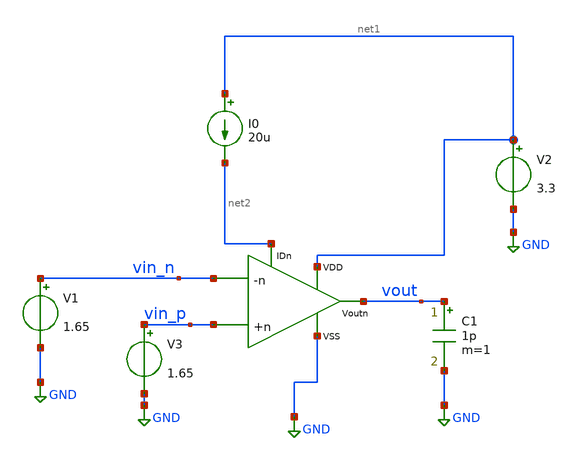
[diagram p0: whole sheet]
** sch_path: xschem/ota_miller/prueba_lazo_abierto_ota_n.sch
**.subckt prueba_lazo_abierto_ota_n
V1 vin_n GND 1.65
V2 net1 GND 3.3
C1 vout GND 1p m=1
V3 vin_p GND 1.65
I0 net1 net2 20u
x1 net1 vout net2 vin_n vin_p GND ota_n_in
**** begin user architecture code


.control
save all
* Coloracion de graficas
set color0=white
set color1=black
set color2=blue
set color3=red
set xbrushwidth=2

* 1. Senoidales en contrafase alrededor de 1.65V (amplitud 50uV para no saturar)
alter @v1[sin] [ 1.65 50u 1k 0 0 180 ]
alter @v3[sin] [ 1.65 50u 1k 0 0 0 ]

* 2. Simular 5 ms con paso de 1 us (5 ciclos de 1 kHz)
tran 1u 5m

* 3. Calcular diferencia de entrada y sus valores pico a pico
let vdiff = v(vin_p) - v(vin_n)
let vdiff_max = vecmax(vdiff)
let vdiff_min = vecmin(vdiff)
let vdiff_pp = vdiff_max - vdiff_min

* 4. Medir pico a pico, valor promedio DC y offset respecto a 1.65V (en 3 ciclos: 2ms a 5ms)
meas tran vout_pp pp v(vout) from=2m to=5m
meas tran vout_dc avg v(vout) from=2m to=5m

let Av0 = vout_pp / vdiff_pp
let Av0_dB = 20 * log10(Av0)
let offset_out = vout_dc - 1.65
let offset_in = offset_out / Av0

echo ========================================
print vdiff_pp
print vout_pp
print Av0
print Av0_dB
print vout_dc
print offset_out
print offset_in
echo ========================================

* 5. Graficas por separado: salida y senal diferencial
plot v(vout) title 'Salida OTA (Lazo Abierto)' xlabel 'Tiempo (s)' ylabel 'Voltaje (V)'
plot vdiff title 'Senal Diferencial de Entrada (V+ - V-)' xlabel 'Tiempo (s)' ylabel 'Voltaje (V)'
.endc




.include /home/ringosinye/eda/pdks/gf180mcuD/libs.tech/ngspice/design.ngspice
.lib /home/ringosinye/eda/pdks/gf180mcuD/libs.tech/ngspice/sm141064.ngspice typical
.param sw_stat_mismatch = 0


**** end user architecture code
**.ends

* expanding   symbol:  ota_n_in.sym # of pins=6
** sym_path: xschem/ota_miller/ota_n_in.sym
** sch_path: xschem/ota_miller/ota_n_in.sch
.subckt ota_n_in VDD Voutn IDn -n +n VSS
*.opin Voutn
*.ipin VSS
*.ipin VDD
*.ipin +n
*.ipin -n
*.ipin IDn
XM1 net2 +n net1 GND nfet_03v3 L=1u W=4.1u nf=1 ad='int((nf+1)/2) * W/nf * 0.18u' as='int((nf+2)/2) * W/nf * 0.18u'
+ pd='2*int((nf+1)/2) * (W/nf + 0.18u)' ps='2*int((nf+2)/2) * (W/nf + 0.18u)' nrd='0.18u / W' nrs='0.18u / W'
+ sa=0 sb=0 sd=0 m=1 par=1
XM2 Voutn -n net1 GND nfet_03v3 L=1u W=4.1u nf=1 ad='int((nf+1)/2) * W/nf * 0.18u' as='int((nf+2)/2) * W/nf * 0.18u'
+ pd='2*int((nf+1)/2) * (W/nf + 0.18u)' ps='2*int((nf+2)/2) * (W/nf + 0.18u)' nrd='0.18u / W' nrs='0.18u / W'
+ sa=0 sb=0 sd=0 m=1 par=1
XM3 net2 net2 VDD VDD pfet_03v3 L=1u W=10u nf=1 ad='int((nf+1)/2) * W/nf * 0.18u' as='int((nf+2)/2) * W/nf * 0.18u'
+ pd='2*int((nf+1)/2) * (W/nf + 0.18u)' ps='2*int((nf+2)/2) * (W/nf + 0.18u)' nrd='0.18u / W' nrs='0.18u / W'
+ sa=0 sb=0 sd=0 m=1 par=1
XM4 Voutn net2 VDD VDD pfet_03v3 L=1u W=10u nf=1 ad='int((nf+1)/2) * W/nf * 0.18u' as='int((nf+2)/2) * W/nf * 0.18u'
+ pd='2*int((nf+1)/2) * (W/nf + 0.18u)' ps='2*int((nf+2)/2) * (W/nf + 0.18u)' nrd='0.18u / W' nrs='0.18u / W'
+ sa=0 sb=0 sd=0 m=1 par=1
XM5 net1 IDn VSS GND nfet_03v3 L=1u W=5u nf=1 ad='int((nf+1)/2) * W/nf * 0.18u' as='int((nf+2)/2) * W/nf * 0.18u'
+ pd='2*int((nf+1)/2) * (W/nf + 0.18u)' ps='2*int((nf+2)/2) * (W/nf + 0.18u)' nrd='0.18u / W' nrs='0.18u / W'
+ sa=0 sb=0 sd=0 m=1 par=1
XM6 IDn IDn VSS GND nfet_03v3 L=1u W=1u nf=1 ad='int((nf+1)/2) * W/nf * 0.18u' as='int((nf+2)/2) * W/nf * 0.18u'
+ pd='2*int((nf+1)/2) * (W/nf + 0.18u)' ps='2*int((nf+2)/2) * (W/nf + 0.18u)' nrd='0.18u / W' nrs='0.18u / W'
+ sa=0 sb=0 sd=0 m=1 par=1
.ends

.GLOBAL GND
.end
